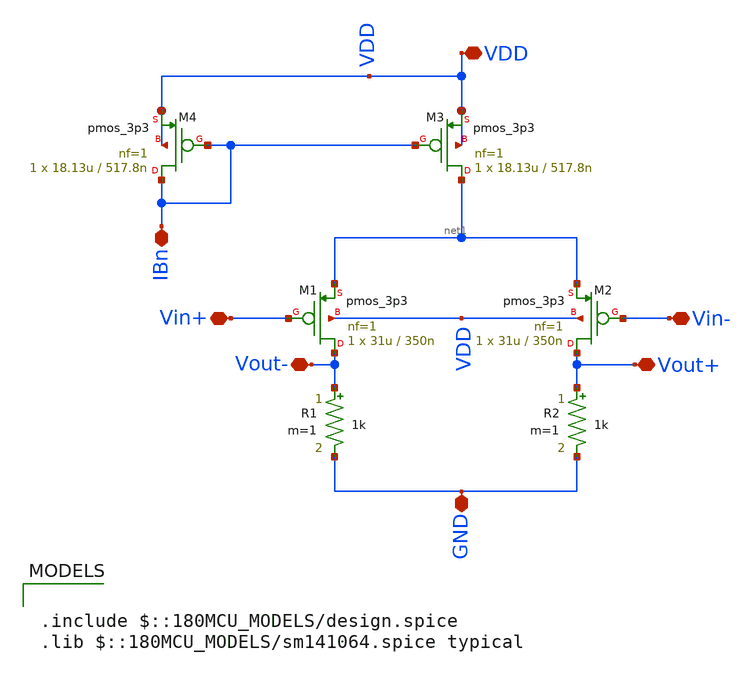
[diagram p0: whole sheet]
** sch_path: ITI_Labs/Lab6/Design/Lab06.sch
**.subckt Lab06 VDD IBn Vin+ Vin- Vout- Vout+ GND
*.iopin VDD
*.iopin IBn
*.iopin Vin+
*.iopin Vin-
*.iopin Vout-
*.iopin Vout+
*.iopin GND
XM1 Vout- Vin+ net1 VDD pmos_3p3 L=350n W=31u nf=1 ad='int((nf+1)/2) * W/nf * 0.18u' as='int((nf+2)/2) * W/nf * 0.18u'
+ pd='2*int((nf+1)/2) * (W/nf + 0.18u)' ps='2*int((nf+2)/2) * (W/nf + 0.18u)' nrd='0.18u / W' nrs='0.18u / W'
+ sa=0 sb=0 sd=0 m=1
XM3 net1 IBn VDD VDD pmos_3p3 L=517.8n W=18.13u nf=1 ad='int((nf+1)/2) * W/nf * 0.18u' as='int((nf+2)/2) * W/nf * 0.18u'
+ pd='2*int((nf+1)/2) * (W/nf + 0.18u)' ps='2*int((nf+2)/2) * (W/nf + 0.18u)' nrd='0.18u / W' nrs='0.18u / W'
+ sa=0 sb=0 sd=0 m=1
R1 Vout- GND 1k m=1
R2 Vout+ GND 1k m=1
XM2 Vout+ Vin- net1 VDD pmos_3p3 L=350n W=31u nf=1 ad='int((nf+1)/2) * W/nf * 0.18u' as='int((nf+2)/2) * W/nf * 0.18u'
+ pd='2*int((nf+1)/2) * (W/nf + 0.18u)' ps='2*int((nf+2)/2) * (W/nf + 0.18u)' nrd='0.18u / W' nrs='0.18u / W'
+ sa=0 sb=0 sd=0 m=1
XM4 IBn IBn VDD VDD pmos_3p3 L=517.8n W=18.13u nf=1 ad='int((nf+1)/2) * W/nf * 0.18u' as='int((nf+2)/2) * W/nf * 0.18u'
+ pd='2*int((nf+1)/2) * (W/nf + 0.18u)' ps='2*int((nf+2)/2) * (W/nf + 0.18u)' nrd='0.18u / W' nrs='0.18u / W'
+ sa=0 sb=0 sd=0 m=1
**** begin user architecture code

.include $::180MCU_MODELS/design.spice
.lib $::180MCU_MODELS/sm141064.spice typical

**** end user architecture code
**.ends
.end
